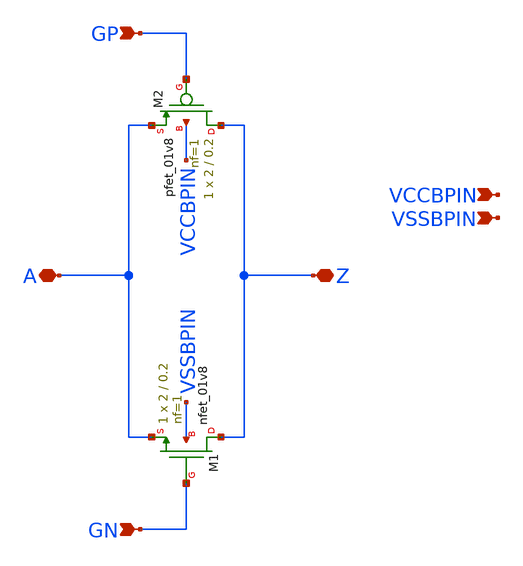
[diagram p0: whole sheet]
** sch_path: xschem/passgate.sch
**.subckt passgate A Z GP GN VCCBPIN VSSBPIN
*.iopin A
*.iopin Z
*.ipin GP
*.ipin GN
*.ipin VCCBPIN
*.ipin VSSBPIN
XM1 Z GN A VSSBPIN sky130_fd_pr__nfet_01v8 L=0.2 W=2 nf=1 ad='int((nf+1)/2) * W/nf * 0.29' as='int((nf+2)/2) * W/nf * 0.29'
+ pd='2*int((nf+1)/2) * (W/nf + 0.29)' ps='2*int((nf+2)/2) * (W/nf + 0.29)' nrd='0.29 / W' nrs='0.29 / W'
+ sa=0 sb=0 sd=0 mult=1 m=1
XM2 Z GP A VCCBPIN sky130_fd_pr__pfet_01v8 L=0.2 W=2 nf=1 ad='int((nf+1)/2) * W/nf * 0.29' as='int((nf+2)/2) * W/nf * 0.29'
+ pd='2*int((nf+1)/2) * (W/nf + 0.29)' ps='2*int((nf+2)/2) * (W/nf + 0.29)' nrd='0.29 / W' nrs='0.29 / W'
+ sa=0 sb=0 sd=0 mult=1 m=1
**.ends
.end
